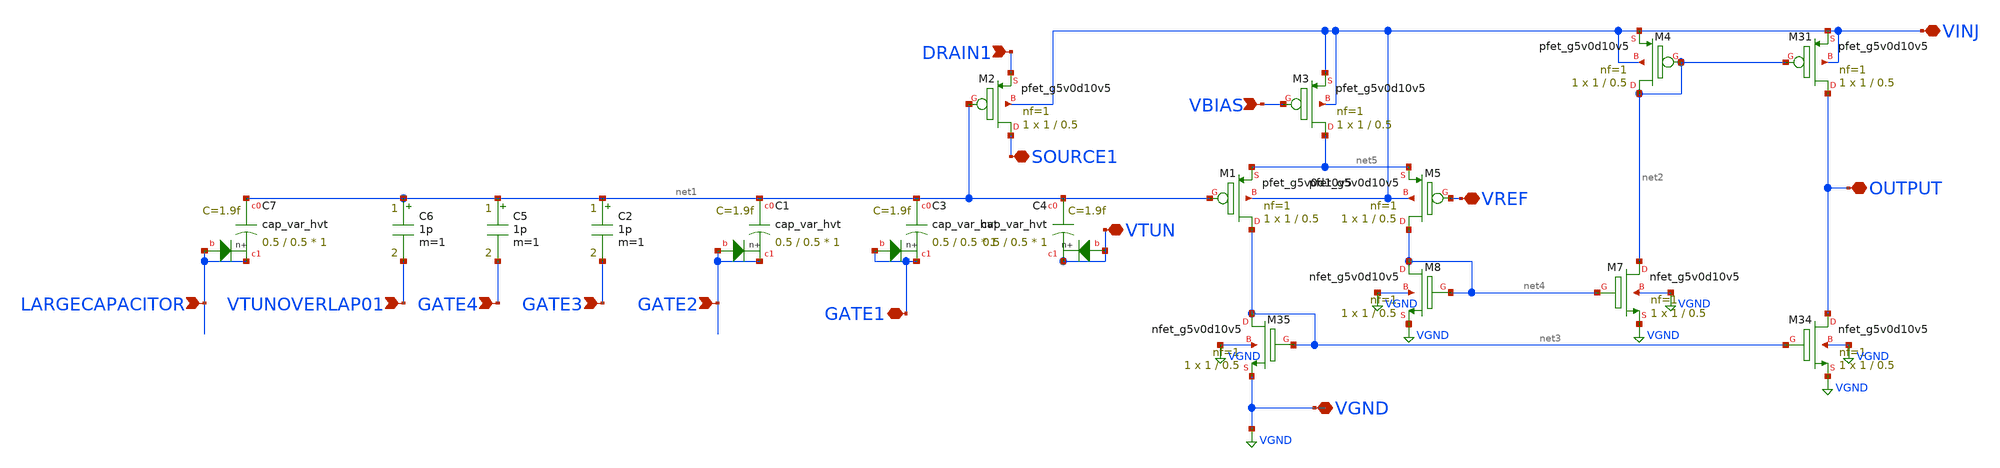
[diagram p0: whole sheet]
** sch_path: libs.ref/sky130_hilas_sc/xschem/sky130_hilas_FGcharacterization01.sch
**.subckt sky130_hilas_FGcharacterization01 VBIAS DRAIN1 GATE3 GATE2 VTUN SOURCE1 VINJ GATE1 OUTPUT
*+ VREF GATE4 VTUNOVERLAP01 VGND LARGECAPACITOR
*.ipin VBIAS
*.ipin DRAIN1
*.ipin GATE3
*.ipin GATE2
*.iopin VTUN
*.iopin SOURCE1
*.iopin VINJ
*.iopin GATE1
*.iopin OUTPUT
*.iopin VREF
*.ipin GATE4
*.ipin VTUNOVERLAP01
*.iopin VGND
*.ipin LARGECAPACITOR
XM3 net5 VBIAS VINJ VINJ sky130_fd_pr__pfet_g5v0d10v5 L=0.5 W=1 nf=1 ad='int((nf+1)/2) * W/nf * 0.29'
+ as='int((nf+2)/2) * W/nf * 0.29' pd='2*int((nf+1)/2) * (W/nf + 0.29)' ps='2*int((nf+2)/2) * (W/nf + 0.29)'
+ nrd='0.29 / W' nrs='0.29 / W' sa=0 sb=0 sd=0 mult=1 m=1
XC1 net1 GATE2 GATE2 sky130_fd_pr__cap_var_hvt W=0.5 L=0.5 VM=1 m=1
XM5 net4 VREF net5 VINJ sky130_fd_pr__pfet_g5v0d10v5 L=0.5 W=1 nf=1 ad='int((nf+1)/2) * W/nf * 0.29'
+ as='int((nf+2)/2) * W/nf * 0.29' pd='2*int((nf+1)/2) * (W/nf + 0.29)' ps='2*int((nf+2)/2) * (W/nf + 0.29)'
+ nrd='0.29 / W' nrs='0.29 / W' sa=0 sb=0 sd=0 mult=1 m=1
XM1 net3 net1 net5 VINJ sky130_fd_pr__pfet_g5v0d10v5 L=0.5 W=1 nf=1 ad='int((nf+1)/2) * W/nf * 0.29'
+ as='int((nf+2)/2) * W/nf * 0.29' pd='2*int((nf+1)/2) * (W/nf + 0.29)' ps='2*int((nf+2)/2) * (W/nf + 0.29)'
+ nrd='0.29 / W' nrs='0.29 / W' sa=0 sb=0 sd=0 mult=1 m=1
XM2 SOURCE1 net1 DRAIN1 VINJ sky130_fd_pr__pfet_g5v0d10v5 L=0.5 W=1 nf=1 ad='int((nf+1)/2) * W/nf * 0.29'
+ as='int((nf+2)/2) * W/nf * 0.29' pd='2*int((nf+1)/2) * (W/nf + 0.29)' ps='2*int((nf+2)/2) * (W/nf + 0.29)'
+ nrd='0.29 / W' nrs='0.29 / W' sa=0 sb=0 sd=0 mult=1 m=1
XC3 net1 GATE1 GATE1 sky130_fd_pr__cap_var_hvt W=0.5 L=0.5 VM=1 m=1
XM4 net2 net2 VINJ VINJ sky130_fd_pr__pfet_g5v0d10v5 L=0.5 W=1 nf=1 ad='int((nf+1)/2) * W/nf * 0.29'
+ as='int((nf+2)/2) * W/nf * 0.29' pd='2*int((nf+1)/2) * (W/nf + 0.29)' ps='2*int((nf+2)/2) * (W/nf + 0.29)'
+ nrd='0.29 / W' nrs='0.29 / W' sa=0 sb=0 sd=0 mult=1 m=1
XC4 net1 VTUN VTUN sky130_fd_pr__cap_var_hvt W=0.5 L=0.5 VM=1 m=1
XM31 OUTPUT net2 VINJ VINJ sky130_fd_pr__pfet_g5v0d10v5 L=0.5 W=1 nf=1 ad='int((nf+1)/2) * W/nf * 0.29'
+ as='int((nf+2)/2) * W/nf * 0.29' pd='2*int((nf+1)/2) * (W/nf + 0.29)' ps='2*int((nf+2)/2) * (W/nf + 0.29)'
+ nrd='0.29 / W' nrs='0.29 / W' sa=0 sb=0 sd=0 mult=1 m=1
XM34 OUTPUT net3 VGND VGND sky130_fd_pr__nfet_g5v0d10v5 L=0.5 W=1 nf=1 ad='int((nf+1)/2) * W/nf * 0.29'
+ as='int((nf+2)/2) * W/nf * 0.29' pd='2*int((nf+1)/2) * (W/nf + 0.29)' ps='2*int((nf+2)/2) * (W/nf + 0.29)'
+ nrd='0.29 / W' nrs='0.29 / W' sa=0 sb=0 sd=0 mult=1 m=1
XM35 net3 net3 VGND VGND sky130_fd_pr__nfet_g5v0d10v5 L=0.5 W=1 nf=1 ad='int((nf+1)/2) * W/nf * 0.29'
+ as='int((nf+2)/2) * W/nf * 0.29' pd='2*int((nf+1)/2) * (W/nf + 0.29)' ps='2*int((nf+2)/2) * (W/nf + 0.29)'
+ nrd='0.29 / W' nrs='0.29 / W' sa=0 sb=0 sd=0 mult=1 m=1
XM7 net2 net4 VGND VGND sky130_fd_pr__nfet_g5v0d10v5 L=0.5 W=1 nf=1 ad='int((nf+1)/2) * W/nf * 0.29'
+ as='int((nf+2)/2) * W/nf * 0.29' pd='2*int((nf+1)/2) * (W/nf + 0.29)' ps='2*int((nf+2)/2) * (W/nf + 0.29)'
+ nrd='0.29 / W' nrs='0.29 / W' sa=0 sb=0 sd=0 mult=1 m=1
XM8 net4 net4 VGND VGND sky130_fd_pr__nfet_g5v0d10v5 L=0.5 W=1 nf=1 ad='int((nf+1)/2) * W/nf * 0.29'
+ as='int((nf+2)/2) * W/nf * 0.29' pd='2*int((nf+1)/2) * (W/nf + 0.29)' ps='2*int((nf+2)/2) * (W/nf + 0.29)'
+ nrd='0.29 / W' nrs='0.29 / W' sa=0 sb=0 sd=0 mult=1 m=1
C2 net1 GATE3 1p m=1
C5 net1 GATE4 1p m=1
C6 net1 VTUNOVERLAP01 1p m=1
XC7 net1 LARGECAPACITOR LARGECAPACITOR sky130_fd_pr__cap_var_hvt W=0.5 L=0.5 VM=1 m=1
**.ends
.GLOBAL VGND
.end
